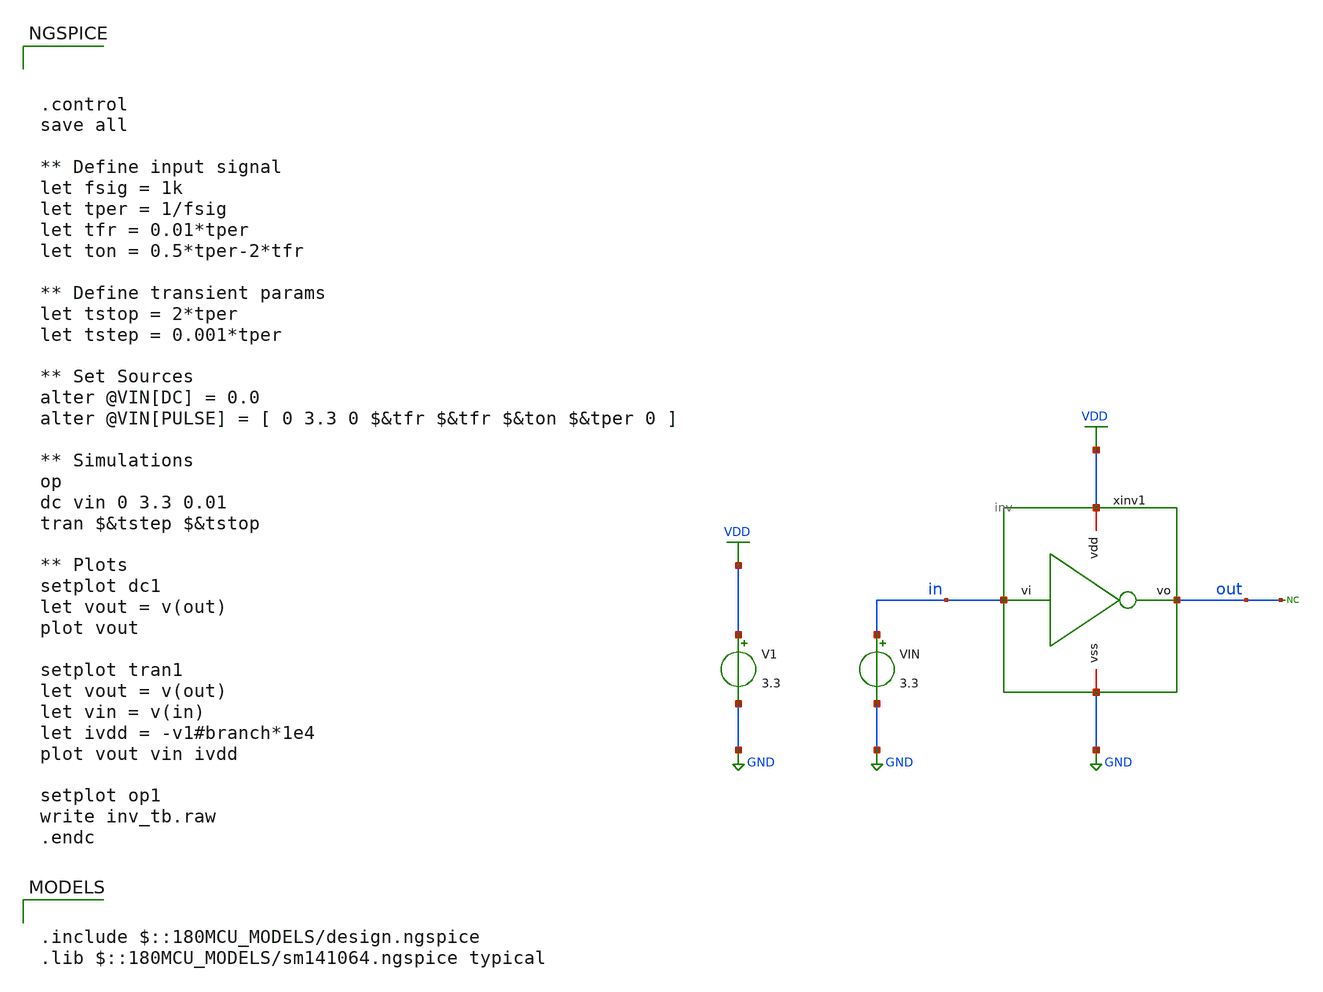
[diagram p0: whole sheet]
** sch_path: _build/images/iic-osic-tools/skel/foss/examples/demo_gf180mcuD/ana/inv_tb.sch
**.subckt inv_tb
xinv1 VDD in out GND inv
V1 VDD GND 3.3
VIN in GND 3.3
* noconn out
**** begin user architecture code

.include $::180MCU_MODELS/design.ngspice
.lib $::180MCU_MODELS/sm141064.ngspice typical




.control
save all

** Define input signal
let fsig = 1k
let tper = 1/fsig
let tfr = 0.01*tper
let ton = 0.5*tper-2*tfr

** Define transient params
let tstop = 2*tper
let tstep = 0.001*tper

** Set Sources
alter @VIN[DC] = 0.0
alter @VIN[PULSE] = [ 0 3.3 0 $&tfr $&tfr $&ton $&tper 0 ]

** Simulations
op
dc vin 0 3.3 0.01
tran $&tstep $&tstop

** Plots
setplot dc1
let vout = v(out)
plot vout

setplot tran1
let vout = v(out)
let vin = v(in)
let ivdd = -v1#branch*1e4
plot vout vin ivdd

setplot op1
write inv_tb.raw
.endc


**** end user architecture code
**.ends

* expanding   symbol:  inv.sym # of pins=4
** sym_path: _build/images/iic-osic-tools/skel_eda/foss/examples/demo_gf180mcuD/ana/inv.sym
** sch_path: _build/images/iic-osic-tools/skel_eda/foss/examples/demo_gf180mcuD/ana/inv.sch
.subckt inv vdd vi vo vss
*.iopin vdd
*.iopin vss
*.ipin vi
*.opin vo
XM1 vo vi vss vss nfet_03v3 L=0.28u W=1u nf=1 ad='int((nf+1)/2) * W/nf * 0.18u' as='int((nf+2)/2) * W/nf * 0.18u'
+ pd='2*int((nf+1)/2) * (W/nf + 0.18u)' ps='2*int((nf+2)/2) * (W/nf + 0.18u)' nrd='0.18u / W' nrs='0.18u / W'
+ sa=0 sb=0 sd=0 m=1
XM2 vo vi vdd vdd pfet_03v3 L=0.28u W=2u nf=1 ad='int((nf+1)/2) * W/nf * 0.18u' as='int((nf+2)/2) * W/nf * 0.18u'
+ pd='2*int((nf+1)/2) * (W/nf + 0.18u)' ps='2*int((nf+2)/2) * (W/nf + 0.18u)' nrd='0.18u / W' nrs='0.18u / W'
+ sa=0 sb=0 sd=0 m=1
.ends

.GLOBAL VDD
.GLOBAL GND
.end
